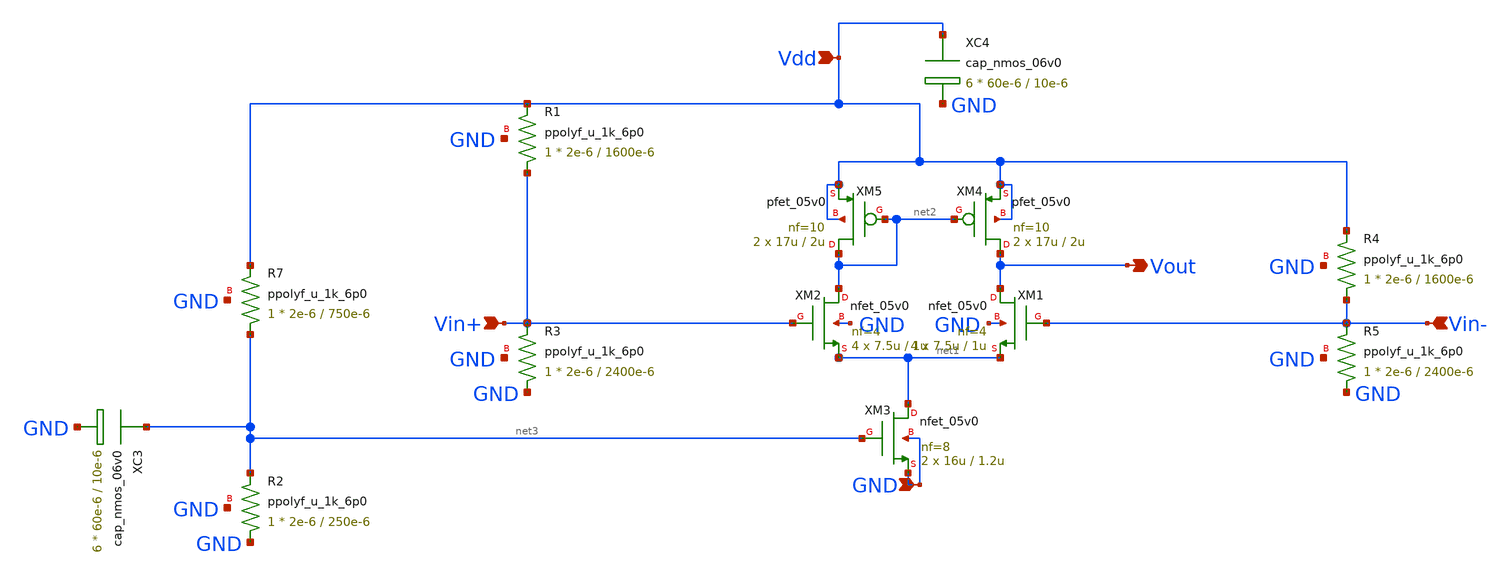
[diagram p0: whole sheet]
** sch_path: RN_Gm3/RN_gm3_ota.sch
**.subckt RN_gm3_ota Vout Vin+ Vin- Vdd GND
*.opin Vout
*.ipin Vin+
*.ipin Vin-
*.ipin Vdd
*.ipin GND
XM3 net1 net3 GND GND nfet_05v0 L=1.2u W=16u nf=8 ad='int((nf+1)/2) * W/nf * 0.18u' as='int((nf+2)/2) * W/nf * 0.18u'
+ pd='2*int((nf+1)/2) * (W/nf + 0.18u)' ps='2*int((nf+2)/2) * (W/nf + 0.18u)' nrd='0.18u / W' nrs='0.18u / W'
+ sa=0 sb=0 sd=0 m=2
XM2 net2 Vin+ net1 GND nfet_05v0 L=1u W=7.5u nf=4 ad='int((nf+1)/2) * W/nf * 0.18u' as='int((nf+2)/2) * W/nf * 0.18u'
+ pd='2*int((nf+1)/2) * (W/nf + 0.18u)' ps='2*int((nf+2)/2) * (W/nf + 0.18u)' nrd='0.18u / W' nrs='0.18u / W'
+ sa=0 sb=0 sd=0 m=4
XM5 net2 net2 Vdd Vdd pfet_05v0 L=2u W=17u nf=10 ad='int((nf+1)/2) * W/nf * 0.18u' as='int((nf+2)/2) * W/nf * 0.18u'
+ pd='2*int((nf+1)/2) * (W/nf + 0.18u)' ps='2*int((nf+2)/2) * (W/nf + 0.18u)' nrd='0.18u / W' nrs='0.18u / W'
+ sa=0 sb=0 sd=0 m=2
XC3 net3 GND cap_nmos_06v0 c_width=60e-6 c_length=10e-6 m=6
XC4 Vdd GND cap_nmos_06v0 c_width=60e-6 c_length=10e-6 m=6
XM1 Vout Vin- net1 GND nfet_05v0 L=1u W=7.5u nf=4 ad='int((nf+1)/2) * W/nf * 0.18u' as='int((nf+2)/2) * W/nf * 0.18u'
+ pd='2*int((nf+1)/2) * (W/nf + 0.18u)' ps='2*int((nf+2)/2) * (W/nf + 0.18u)' nrd='0.18u / W' nrs='0.18u / W'
+ sa=0 sb=0 sd=0 m=4
XM4 Vout net2 Vdd Vdd pfet_05v0 L=2u W=17u nf=10 ad='int((nf+1)/2) * W/nf * 0.18u' as='int((nf+2)/2) * W/nf * 0.18u'
+ pd='2*int((nf+1)/2) * (W/nf + 0.18u)' ps='2*int((nf+2)/2) * (W/nf + 0.18u)' nrd='0.18u / W' nrs='0.18u / W'
+ sa=0 sb=0 sd=0 m=2
XR2 GND net3 GND ppolyf_u_1k_6p0 r_width=2e-6 r_length=250e-6 m=1
XR7 net3 Vdd GND ppolyf_u_1k_6p0 r_width=2e-6 r_length=750e-6 m=1
XR1 Vin+ Vdd GND ppolyf_u_1k_6p0 r_width=2e-6 r_length=1600e-6 m=1
XR3 GND Vin+ GND ppolyf_u_1k_6p0 r_width=2e-6 r_length=2400e-6 m=1
XR4 Vin- Vdd GND ppolyf_u_1k_6p0 r_width=2e-6 r_length=1600e-6 m=1
XR5 GND Vin- GND ppolyf_u_1k_6p0 r_width=2e-6 r_length=2400e-6 m=1
**.ends
.end
